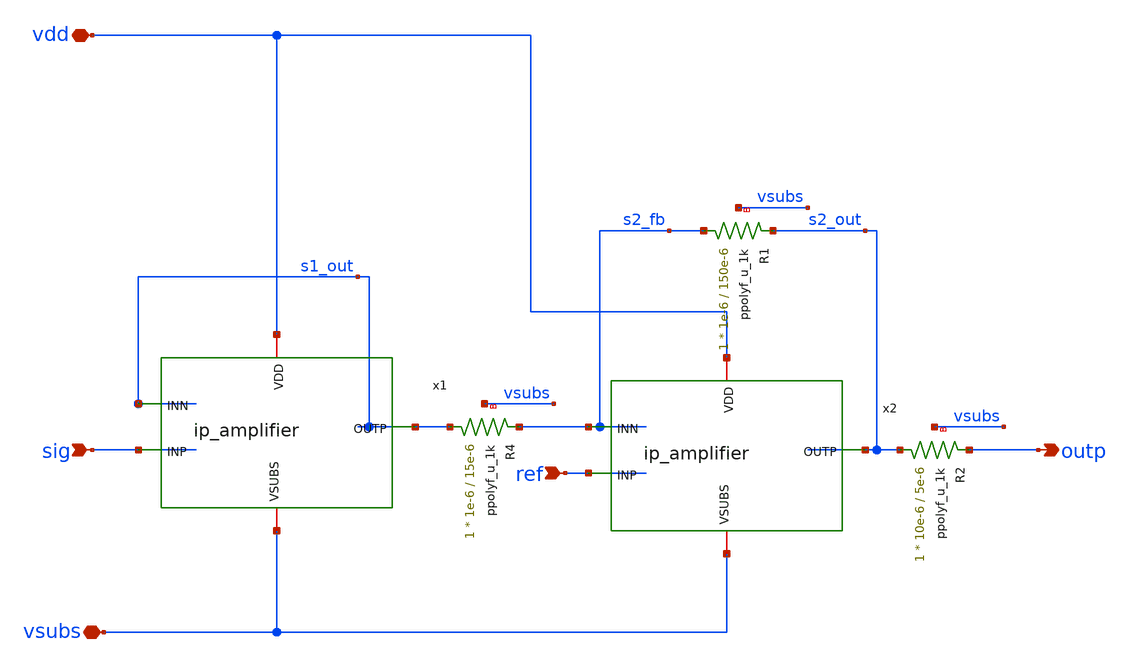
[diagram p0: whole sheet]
** sch_path: xschem/ip_sigproc.sch
**.subckt ip_sigproc sig ref vdd vsubs outp
*.ipin sig
*.ipin ref
*.iopin vdd
*.iopin vsubs
*.opin outp
x1 vdd s1_out sig s1_out vsubs ip_amplifier
x2 vdd s2_out ref s2_fb vsubs ip_amplifier
XR4 s1_out s2_fb vsubs ppolyf_u_1k r_width=1e-6 r_length=15e-6 m=1
XR1 s2_fb s2_out vsubs ppolyf_u_1k r_width=1e-6 r_length=150e-6 m=1
XR2 s2_out outp vsubs ppolyf_u_1k r_width=10e-6 r_length=5e-6 m=1
**.ends

* expanding   symbol:  ip_amplifier.sym # of pins=5
** sym_path: xschem/ip_amplifier.sym
** sch_path: xschem/ip_amplifier.sch
.subckt ip_amplifier VDD OUTP INP INN VSUBS
*.iopin VDD
*.iopin VSUBS
*.ipin INP
*.ipin INN
*.opin OUTP
XM1 COMP INP COMMON_ VDD pfet_03v3 L=5u W=18.0u nf=1 ad='int((nf+1)/2) * W/nf * 0.18u' as='int((nf+2)/2) * W/nf * 0.18u'
+ pd='2*int((nf+1)/2) * (W/nf + 0.18u)' ps='2*int((nf+2)/2) * (W/nf + 0.18u)' nrd='0.18u / W' nrs='0.18u / W'
+ sa=0 sb=0 sd=0 m=1 par=1
XM2 net6 INN COMMON_ VDD pfet_03v3 L=5u W=18.0u nf=1 ad='int((nf+1)/2) * W/nf * 0.18u' as='int((nf+2)/2) * W/nf * 0.18u'
+ pd='2*int((nf+1)/2) * (W/nf + 0.18u)' ps='2*int((nf+2)/2) * (W/nf + 0.18u)' nrd='0.18u / W' nrs='0.18u / W'
+ sa=0 sb=0 sd=0 m=1 par=1
XM3 net2 NBIAS VSUBS vsubs nfet_03v3 L=2u W=6u nf=1 ad='int((nf+1)/2) * W/nf * 0.18u' as='int((nf+2)/2) * W/nf * 0.18u'
+ pd='2*int((nf+1)/2) * (W/nf + 0.18u)' ps='2*int((nf+2)/2) * (W/nf + 0.18u)' nrd='0.18u / W' nrs='0.18u / W'
+ sa=0 sb=0 sd=0 m=2 par=2
XM4 net1 NBIAS VSUBS vsubs nfet_03v3 L=2u W=6u nf=1 ad='int((nf+1)/2) * W/nf * 0.18u' as='int((nf+2)/2) * W/nf * 0.18u'
+ pd='2*int((nf+1)/2) * (W/nf + 0.18u)' ps='2*int((nf+2)/2) * (W/nf + 0.18u)' nrd='0.18u / W' nrs='0.18u / W'
+ sa=0 sb=0 sd=0 m=1 par=1
XM7 NBIAS NBIAS net2 vsubs nfet_03v3 L=0.5u W=6u nf=1 ad='int((nf+1)/2) * W/nf * 0.18u' as='int((nf+2)/2) * W/nf * 0.18u'
+ pd='2*int((nf+1)/2) * (W/nf + 0.18u)' ps='2*int((nf+2)/2) * (W/nf + 0.18u)' nrd='0.18u / W' nrs='0.18u / W'
+ sa=0 sb=0 sd=0 m=4 par=4
XM8 net3 NBIAS net1 vsubs nfet_03v3 L=0.5u W=6u nf=1 ad='int((nf+1)/2) * W/nf * 0.18u' as='int((nf+2)/2) * W/nf * 0.18u'
+ pd='2*int((nf+1)/2) * (W/nf + 0.18u)' ps='2*int((nf+2)/2) * (W/nf + 0.18u)' nrd='0.18u / W' nrs='0.18u / W'
+ sa=0 sb=0 sd=0 m=4 par=4
XM9 net4 PBIAS VDD VDD pfet_03v3 L=2u W=6u nf=1 ad='int((nf+1)/2) * W/nf * 0.18u' as='int((nf+2)/2) * W/nf * 0.18u'
+ pd='2*int((nf+1)/2) * (W/nf + 0.18u)' ps='2*int((nf+2)/2) * (W/nf + 0.18u)' nrd='0.18u / W' nrs='0.18u / W'
+ sa=0 sb=0 sd=0 m=1 par=1
XM10 net5 PBIAS VDD VDD pfet_03v3 L=2u W=6u nf=1 ad='int((nf+1)/2) * W/nf * 0.18u' as='int((nf+2)/2) * W/nf * 0.18u'
+ pd='2*int((nf+1)/2) * (W/nf + 0.18u)' ps='2*int((nf+2)/2) * (W/nf + 0.18u)' nrd='0.18u / W' nrs='0.18u / W'
+ sa=0 sb=0 sd=0 m=1 par=1
XM11 PBIAS PBIAS net4 VDD pfet_03v3 L=0.5u W=6u nf=1 ad='int((nf+1)/2) * W/nf * 0.18u' as='int((nf+2)/2) * W/nf * 0.18u'
+ pd='2*int((nf+1)/2) * (W/nf + 0.18u)' ps='2*int((nf+2)/2) * (W/nf + 0.18u)' nrd='0.18u / W' nrs='0.18u / W'
+ sa=0 sb=0 sd=0 m=4 par=4
XM12 COMMON PBIAS net5 VDD pfet_03v3 L=0.5u W=6u nf=1 ad='int((nf+1)/2) * W/nf * 0.18u' as='int((nf+2)/2) * W/nf * 0.18u'
+ pd='2*int((nf+1)/2) * (W/nf + 0.18u)' ps='2*int((nf+2)/2) * (W/nf + 0.18u)' nrd='0.18u / W' nrs='0.18u / W'
+ sa=0 sb=0 sd=0 m=4 par=4
XM13 COMP net6 VSUBS vsubs nfet_03v3 L=5u W=6u nf=1 ad='int((nf+1)/2) * W/nf * 0.18u' as='int((nf+2)/2) * W/nf * 0.18u'
+ pd='2*int((nf+1)/2) * (W/nf + 0.18u)' ps='2*int((nf+2)/2) * (W/nf + 0.18u)' nrd='0.18u / W' nrs='0.18u / W'
+ sa=0 sb=0 sd=0 m=1 par=1
XM14 net6 net6 VSUBS vsubs nfet_03v3 L=5u W=6u nf=1 ad='int((nf+1)/2) * W/nf * 0.18u' as='int((nf+2)/2) * W/nf * 0.18u'
+ pd='2*int((nf+1)/2) * (W/nf + 0.18u)' ps='2*int((nf+2)/2) * (W/nf + 0.18u)' nrd='0.18u / W' nrs='0.18u / W'
+ sa=0 sb=0 sd=0 m=1 par=1
XM17 net8 PBIAS VDD VDD pfet_03v3 L=0.5u W=12u nf=1 ad='int((nf+1)/2) * W/nf * 0.18u' as='int((nf+2)/2) * W/nf * 0.18u'
+ pd='2*int((nf+1)/2) * (W/nf + 0.18u)' ps='2*int((nf+2)/2) * (W/nf + 0.18u)' nrd='0.18u / W' nrs='0.18u / W'
+ sa=0 sb=0 sd=0 m=2 par=2
XM18 OUTP COMP VSUBS vsubs nfet_03v3 L=0.5u W=12u nf=1 ad='int((nf+1)/2) * W/nf * 0.18u' as='int((nf+2)/2) * W/nf * 0.18u'
+ pd='2*int((nf+1)/2) * (W/nf + 0.18u)' ps='2*int((nf+2)/2) * (W/nf + 0.18u)' nrd='0.18u / W' nrs='0.18u / W'
+ sa=0 sb=0 sd=0 m=4 par=4
XR3 NBIAS net7 vsubs ppolyf_u_1k r_width=1e-6 r_length=48e-6 m=1
Vmeas VDD net7 0
Vmeas1 PBIAS net3 0
XC1 OUTP net9 cap_pmos_03v3 c_width=13.5e-6 c_length=18e-6 m=1
XC2 COMP net9 cap_pmos_03v3 c_width=13.5e-6 c_length=18e-6 m=1
Vmeas2 COMMON COMMON_ 0
Vmeas3 net8 OUTP 0
XR2 VDD net9 vsubs ppolyf_u_1k r_width=1e-6 r_length=96e-6 m=1
.ends

.end
